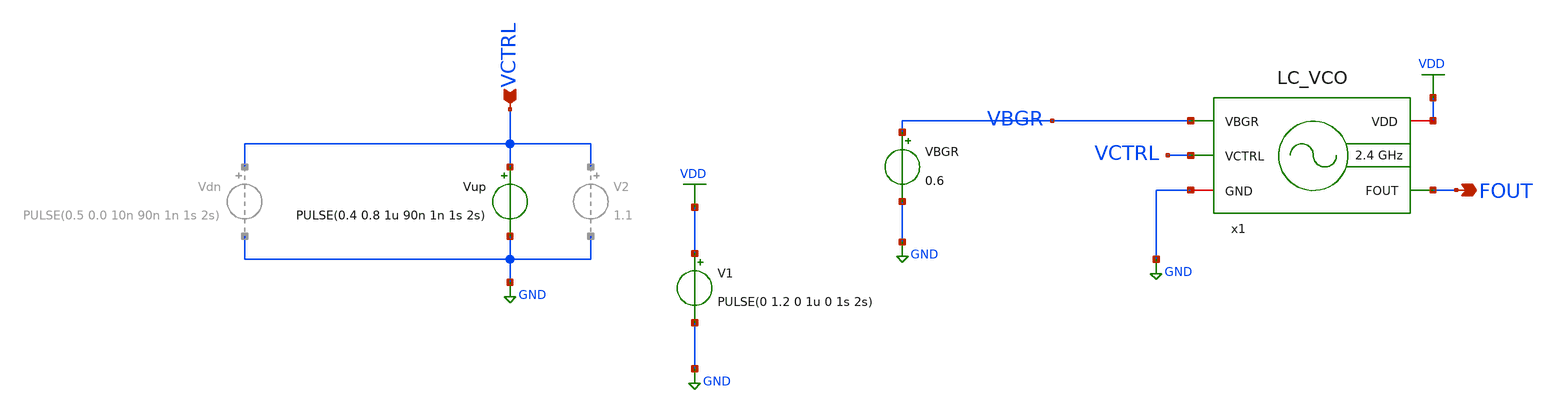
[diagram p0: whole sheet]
** sch_path: xschem/lc-vco/LC_VCO_tb.sch
**.subckt LC_VCO_tb FOUT VCTRL
*.opin FOUT
*.ipin VCTRL
V1 VDD GND PULSE(0 1.2 0 1u 0 1s 2s)
Vup VCTRL GND PULSE(0.4 0.8 1u 90n 1n 1s 2s)
VBGR VBGR GND 0.6
x1 VDD VCTRL GND FOUT VBGR LC_VCO
**** begin user architecture code



.param temp = 27
.options method=gear rshunt=1.0e12

.control

* Save required signals
save v(VCTRL) v(FOUT) v(x1.Vx) v(x1.OUTp) v(VBGR)

* Long transient simulation
tran 10p 2u

* Save raw waveform
write LC_VCO_standalone_tran.raw

* Plot transient waveform
let vout = v(FOUT)
plot v(VCTRL) v(x1.Vx) v(FOUT) v(x1.OUTp) v(VBGR)
plot v(VBGR)

* Plot steady-state waveform
plot v(VCTRL) v(x1.Vx) v(OUT) v(x1.OUTp) v(VBGR) xlimit 4000n 4005n

* FFT analysis
setplot tran1
linearize vout
set specwindow=blackman
fft vout

* Plot FFT spectrum
let power_out_db = db(vout)
plot power_out_db xlimit 2.34G 2.54G ylimit -200 0

* Find the maximum magnitude value between 2G and 3G
meas sp max_power_out_db max power_out_db FROM=2G TO=3G

* Save FFT spectrum as raw file
write LC_VCO_fft.raw

* Save FFT data
wrdata fft_output_standalone.txt frequency power_out_db

* Save waveform for external processing
wrdata vco_waveform_standalone.txt power_out_db

.endc






.param temp=27
.control
save all
op
write LC_VCO_tb.raw
.endc




.include 4nH_INDUCTOR.spice


.lib cornerMOSlv.lib mos_tt
.lib cornerMOShv.lib mos_tt
.lib cornerRES.lib res_typ
.lib cornerCAP.lib cap_typ

**** end user architecture code
**.ends

* expanding   symbol:  xschem/lc-vco/LC_VCO.sym # of pins=5
** sym_path: xschem/lc-vco/LC_VCO.sym
** sch_path: xschem/lc-vco/LC_VCO.sch
.subckt LC_VCO VDD VCTRL GND FOUT VBGR
*.opin FOUT
*.ipin VCTRL
*.ipin VBGR
*.iopin VDD
*.iopin GND
XM5 Vx Vgs GND GND sg13_lv_nmos w=384u l=1u ng=48 m=1 mm_ok=1
XM4 OUTp OUTn VDD VDD sg13_lv_pmos w=36u l=0.13u ng=5 m=1 mm_ok=1
XM3 OUTn OUTp VDD VDD sg13_lv_pmos w=36u l=0.13u ng=5 m=1 mm_ok=1
XM2 OUTp OUTn Vx GND sg13_lv_nmos w=22u l=0.13u ng=3 m=1 mm_ok=1
XM1 OUTn OUTp Vx GND sg13_lv_nmos w=22u l=0.13u ng=3 m=1 mm_ok=1
XM6 Vgs Vgs GND GND sg13_lv_nmos w=64u l=1u ng=8 m=1 mm_ok=1
XC1 OUTn OUTp GND cap_rfcmim w=21.9e-6 l=21.9e-6 wfeed=10.0e-6 m=1 mm_ok=1
XC3 OUTp VCTRL OUTn GND sg13_hv_svaricap w=9.74u l=0.8u Nx=7
XC2 OUTp VCTRL OUTn GND sg13_hv_svaricap w=9.74u l=0.8u Nx=7
XM7 Vgs VBGR VDD VDD sg13_lv_pmos w=38u l=1u ng=5 m=1 mm_ok=1
XM8 FOUT OUTp VDD VDD sg13_lv_pmos w=15u l=0.13u ng=10 m=1 mm_ok=1
XM9 FOUT OUTp GND GND sg13_lv_nmos w=1.5u l=0.13u ng=1 m=1 mm_ok=1
XM10 net1 OUTn VDD VDD sg13_lv_pmos w=15u l=0.13u ng=10 m=1 mm_ok=1
XM11 net1 OUTn GND GND sg13_lv_nmos w=1.5u l=0.13u ng=1 m=1 mm_ok=1
**** begin user architecture code


.subckt 4nH_INDUCTOR 1 2
* LVS black-box stub only
* Full model is available in 4nH_INDUCTOR.spice
.ends


**** end user architecture code
x2 OUTn OUTp 4nH_INDUCTOR
.ends

.GLOBAL GND
.GLOBAL VDD
.end
